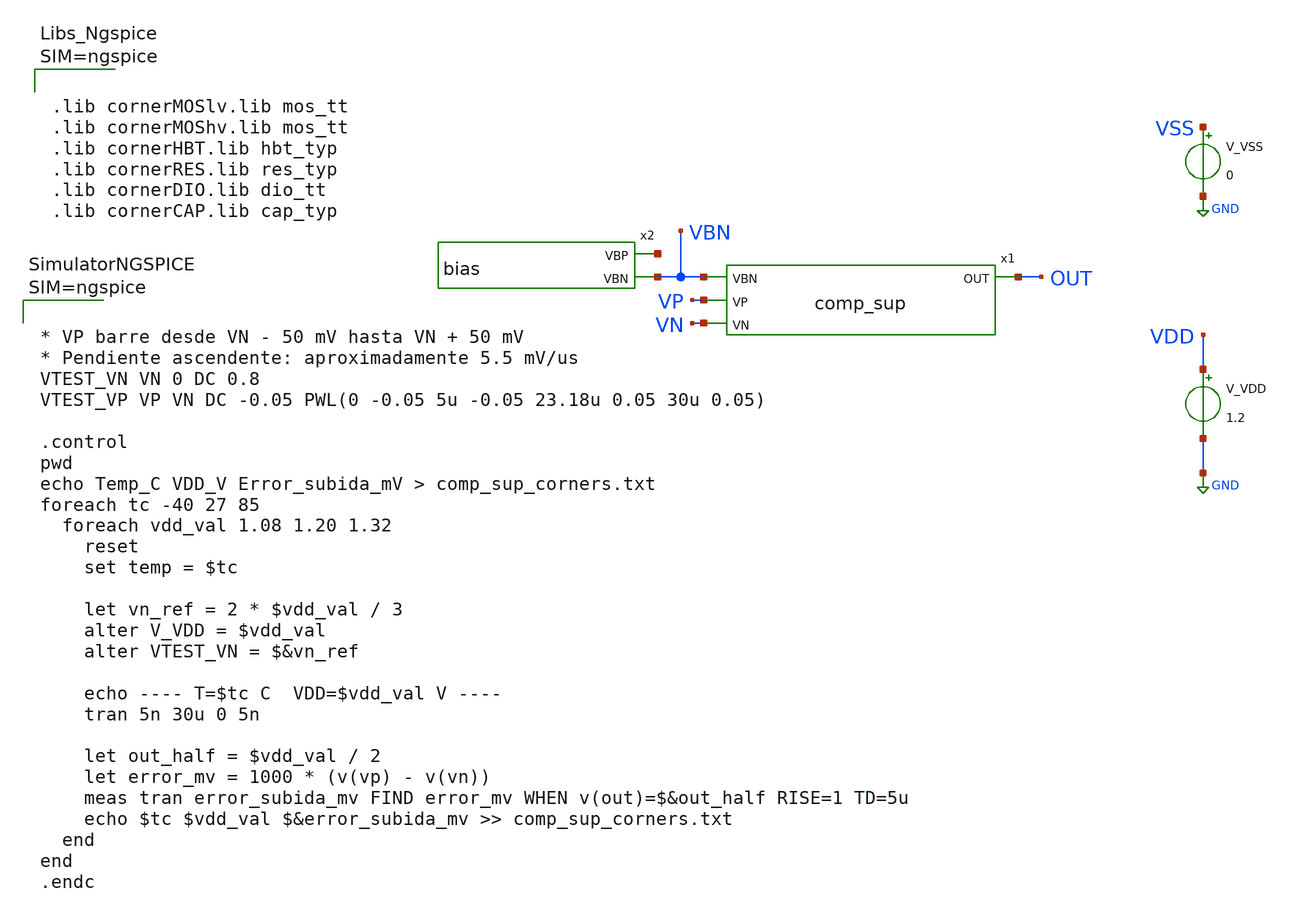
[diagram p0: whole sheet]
** sch_path: design/blocks/comparator/schematic/comp_sup_tb.sch
**.subckt comp_sup_tb
x1 VBN VP VN OUT VDD VSS comp_sup
x2 net1 VBN VDD VSS bias
V_VDD VDD GND 1.2
V_VSS VSS GND 0
**** begin user architecture code



.lib cornerMOSlv.lib mos_tt
.lib cornerMOShv.lib mos_tt
.lib cornerHBT.lib hbt_typ
.lib cornerRES.lib res_typ
.lib cornerDIO.lib dio_tt
.lib cornerCAP.lib cap_typ






* VP barre desde VN - 50 mV hasta VN + 50 mV
* Pendiente ascendente: aproximadamente 5.5 mV/us
VTEST_VN VN 0 DC 0.8
VTEST_VP VP VN DC -0.05 PWL(0 -0.05 5u -0.05 23.18u 0.05 30u 0.05)

.control
pwd
echo Temp_C VDD_V Error_subida_mV > comp_sup_corners.txt
foreach tc -40 27 85
  foreach vdd_val 1.08 1.20 1.32
    reset
    set temp = $tc

    let vn_ref = 2 * $vdd_val / 3
    alter V_VDD = $vdd_val
    alter VTEST_VN = $&vn_ref

    echo ---- T=$tc C  VDD=$vdd_val V ----
    tran 5n 30u 0 5n

    let out_half = $vdd_val / 2
    let error_mv = 1000 * (v(vp) - v(vn))
    meas tran error_subida_mv FIND error_mv WHEN v(out)=$&out_half RISE=1 TD=5u
    echo $tc $vdd_val $&error_subida_mv >> comp_sup_corners.txt
  end
end
.endc


**** end user architecture code
**.ends

* expanding   symbol:  comp_sup.sym # of pins=4
** sym_path: design/blocks/comparator/schematic/comp_sup.sym
** sch_path: design/blocks/comparator/schematic/comp_sup.sch
.subckt comp_sup VBN VP VN OUT VDD VSS
*.opin OUT
*.ipin VN
*.ipin VP
*.ipin VBN
XM2 net1 net1 VDD VDD sg13_lv_pmos w=8u l=1u ng=1 m=1 mm_ok=1
XM3 net3 net1 VDD VDD sg13_lv_pmos w=8u l=1u ng=1 m=1 mm_ok=1
XM4 net1 VP net2 VSS sg13_lv_nmos w=20u l=0.5u ng=3 m=1 mm_ok=1
XM5 net3 VN net2 VSS sg13_lv_nmos w=20u l=0.5u ng=3 m=1 mm_ok=1
XM6 net2 VBN VSS VSS sg13_lv_nmos w=2u l=1u ng=1 m=1 mm_ok=1
x1 net4 net3 VDD VSS sg13g2_inv_1
x2 OUT net4 VDD VSS sg13g2_inv_1
.ends


* expanding   symbol:  bias.sym # of pins=2
** sym_path: design/blocks/bias/schematic/bias.sym
** sch_path: design/blocks/bias/schematic/bias.sch
.subckt bias VBP VBN VDD VSS
*.opin VBP
*.opin VBN
XM1 VBN VBN VSS VSS sg13_lv_nmos w=2u l=1u ng=1 m=1 mm_ok=1
XM2 VBP VBP VDD VDD sg13_lv_pmos w=2u l=1u ng=1 m=1 mm_ok=1
XR2 VBP VSS VSS rhigh w=0.5e-6 l=10.0e-6 m=1 b=0 mm_ok=1
XR1 VDD VBN VSS rhigh w=0.5e-6 l=10.0e-6 m=1 b=0 mm_ok=1
XC1 VBN VSS cap_cmim w=26.0e-6 l=26.0e-6 m=1 mm_ok=1
XC2 VDD VBP cap_cmim w=26.0e-6 l=26.0e-6 m=1 mm_ok=1
.ends


* expanding   symbol:  sg13g2_inv_1.sym # of pins=2
** sym_path: sg13g2_inv_1.sym
** sch_path: sg13g2_inv_1.sch
.subckt sg13g2_inv_1 Y A VDD VSS
*.opin Y
*.ipin A
*.iopin VDD
*.iopin VSS
XM1 Y A VSS VSS sg13_lv_nmos w=740.00n l=130.00n ng=1 m=1 mm_ok=1
XM2 Y A VDD VDD sg13_lv_pmos w=1.12u l=130.00n ng=1 m=1 mm_ok=1
.ends

.GLOBAL GND
.end
